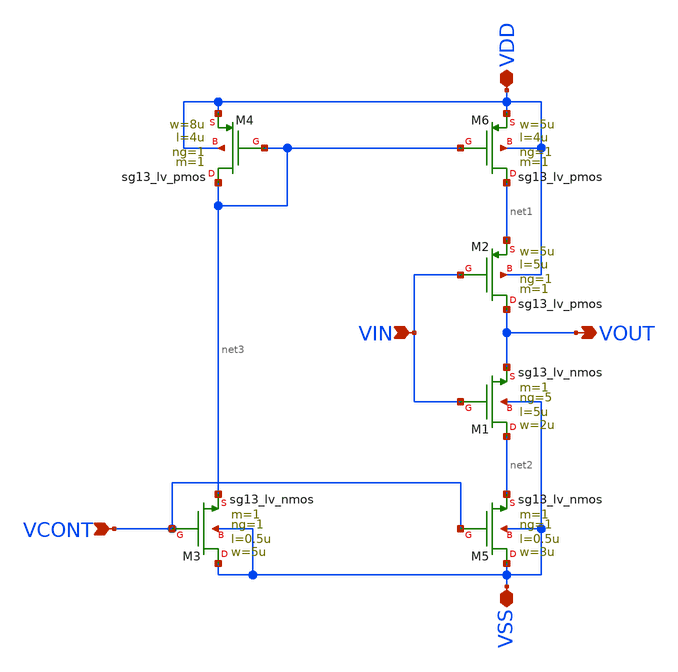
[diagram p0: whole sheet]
** sch_path: DelayLine/others/Delay-Line.sch
**.subckt Delay-Line VIN VOUT VDD VSS VCONT
*.ipin VIN
*.opin VOUT
*.iopin VDD
*.iopin VSS
*.ipin VCONT
XM3 VSS VCONT net3 VSS sg13_lv_nmos w=5u l=0.5u ng=1 m=1 mm_ok=1
XM5 VSS VCONT net2 VSS sg13_lv_nmos w=3u l=0.5u ng=1 m=1 mm_ok=1
XM4 net3 net3 VDD VDD sg13_lv_pmos w=8u l=4u ng=1 m=1 mm_ok=1
XM6 net1 net3 VDD VDD sg13_lv_pmos w=5u l=4u ng=1 m=1 mm_ok=1
XM2 VOUT VIN net1 VDD sg13_lv_pmos w=5u l=5u ng=1 m=1 mm_ok=1
XM1 net2 VIN VOUT VSS sg13_lv_nmos w=2u l=5u ng=5 m=1 mm_ok=1
**.ends
.end
